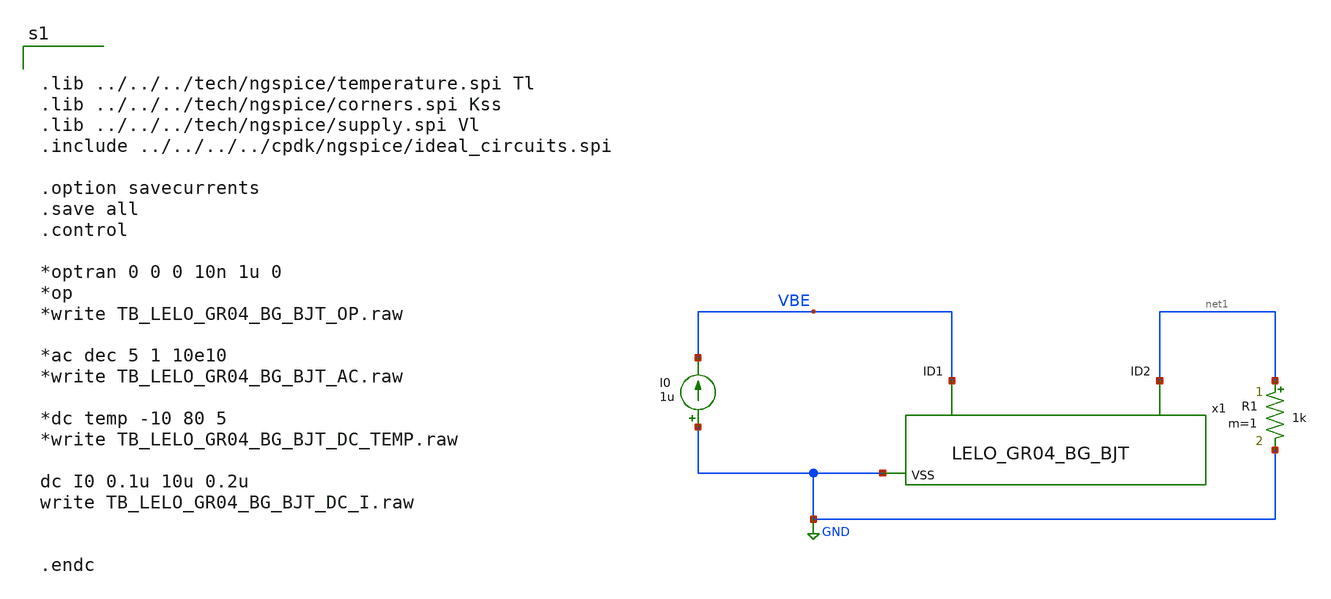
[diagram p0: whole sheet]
** sch_path: design/LELO_GR04_SKY130A/TB_LELO_GR04_BG_BJT.sch
**.subckt TB_LELO_GR04_BG_BJT
x1 VBE net1 GND LELO_GR04_BG_BJT
I0 GND VBE 1u
R1 net1 GND 1k m=1
**** begin user architecture code


.lib ../../../tech/ngspice/temperature.spi Tl
.lib ../../../tech/ngspice/corners.spi Kss
.lib ../../../tech/ngspice/supply.spi Vl
.include ../../../../cpdk/ngspice/ideal_circuits.spi

.option savecurrents
.save all
.control

*optran 0 0 0 10n 1u 0
*op
*write TB_LELO_GR04_BG_BJT_OP.raw

*ac dec 5 1 10e10
*write TB_LELO_GR04_BG_BJT_AC.raw

*dc temp -10 80 5
*write TB_LELO_GR04_BG_BJT_DC_TEMP.raw

dc I0 0.1u 10u 0.2u
write TB_LELO_GR04_BG_BJT_DC_I.raw


.endc


**** end user architecture code
**.ends

* expanding   symbol:  LELO_GR04_SKY130A/LELO_GR04_BG_BJT.sym # of pins=3
** sym_path: design/LELO_GR04_SKY130A/LELO_GR04_BG_BJT.sym
** sch_path: design/LELO_GR04_SKY130A/LELO_GR04_BG_BJT.sch
.subckt LELO_GR04_BG_BJT ID1 ID2 VSS
*.ipin VSS
*.ipin ID1
*.ipin ID2
XQ1 VSS VSS ID1 sky130_fd_pr__pnp_05v5_W3p40L3p40 m=1
XQ2[7] VSS VSS ID2 sky130_fd_pr__pnp_05v5_W3p40L3p40 m=1
XQ2[6] VSS VSS ID2 sky130_fd_pr__pnp_05v5_W3p40L3p40 m=1
XQ2[5] VSS VSS ID2 sky130_fd_pr__pnp_05v5_W3p40L3p40 m=1
XQ2[4] VSS VSS ID2 sky130_fd_pr__pnp_05v5_W3p40L3p40 m=1
XQ2[3] VSS VSS ID2 sky130_fd_pr__pnp_05v5_W3p40L3p40 m=1
XQ2[2] VSS VSS ID2 sky130_fd_pr__pnp_05v5_W3p40L3p40 m=1
XQ2[1] VSS VSS ID2 sky130_fd_pr__pnp_05v5_W3p40L3p40 m=1
XQ2[0] VSS VSS ID2 sky130_fd_pr__pnp_05v5_W3p40L3p40 m=1
.ends

.GLOBAL GND
.end
